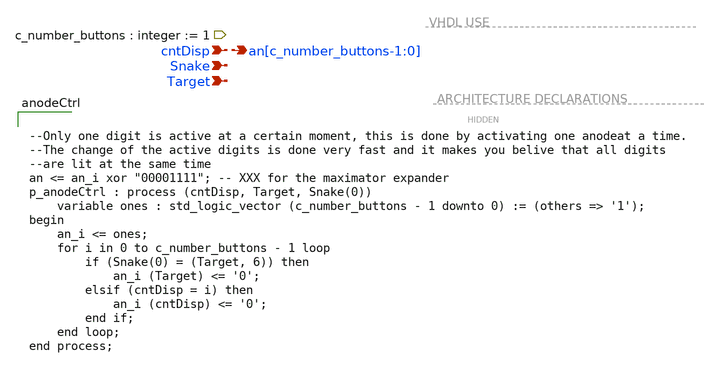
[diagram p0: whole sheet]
** sch_path: xschem/anodeCtrl.sch
**.subckt anodeCtrl Target cntDisp Snake an[c_number_buttons-1:0]
*.ipin Target
*.ipin cntDisp
*.ipin Snake
*.opin an[c_number_buttons-1:0]
**** begin user architecture code


--Only one digit is active at a certain moment, this is done by activating one anodeat a time.
--The change of the active digits is done very fast and it makes you belive that all digits
--are lit at the same time
an <= an_i xor "00001111"; -- XXX for the maximator expander
p_anodeCtrl : process (cntDisp, Target, Snake(0))
	variable ones : std_logic_vector (c_number_buttons - 1 downto 0) := (others => '1');
begin
	an_i <= ones;
	for i in 0 to c_number_buttons - 1 loop
		if (Snake(0) = (Target, 6)) then
			an_i (Target) <= '0';
		elsif (cntDisp = i) then
			an_i (cntDisp) <= '0';
		end if;
	end loop;
end process;


**** end user architecture code
**.ends
.end
